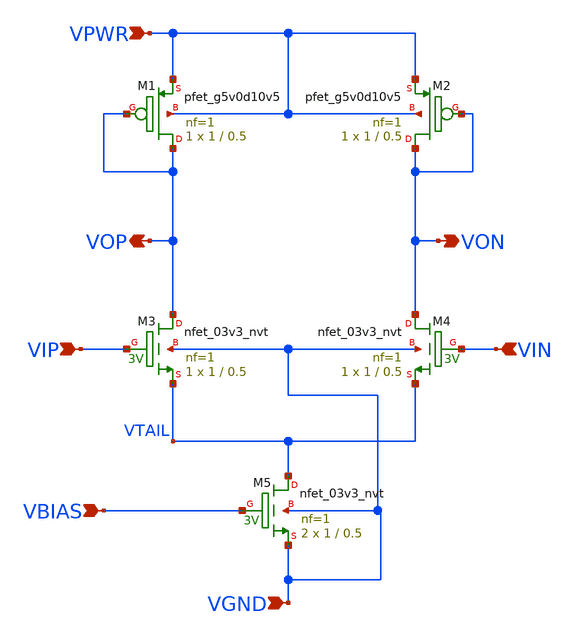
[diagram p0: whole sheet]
** sch_path: xschem/gm-c_filter/ltp.sch
**.subckt ltp VBIAS VIP VPWR VIN VGND VON VOP
*.ipin VBIAS
*.ipin VIP
*.ipin VPWR
*.ipin VIN
*.ipin VGND
*.opin VON
*.opin VOP
XM1 VOP VOP VPWR VPWR sky130_fd_pr__pfet_g5v0d10v5 L=0.5 W=1 nf=1 ad='int((nf+1)/2) * W/nf * 0.29' as='int((nf+2)/2) * W/nf * 0.29'
+ pd='2*int((nf+1)/2) * (W/nf + 0.29)' ps='2*int((nf+2)/2) * (W/nf + 0.29)' nrd='0.29 / W' nrs='0.29 / W'
+ sa=0 sb=0 sd=0 mult=1 m=1
XM2 VON VON VPWR VPWR sky130_fd_pr__pfet_g5v0d10v5 L=0.5 W=1 nf=1 ad='int((nf+1)/2) * W/nf * 0.29' as='int((nf+2)/2) * W/nf * 0.29'
+ pd='2*int((nf+1)/2) * (W/nf + 0.29)' ps='2*int((nf+2)/2) * (W/nf + 0.29)' nrd='0.29 / W' nrs='0.29 / W'
+ sa=0 sb=0 sd=0 mult=1 m=1
XM3 VOP VIP VTAIL VGND sky130_fd_pr__nfet_03v3_nvt L=0.5 W=1 nf=1 ad='int((nf+1)/2) * W/nf * 0.29' as='int((nf+2)/2) * W/nf * 0.29'
+ pd='2*int((nf+1)/2) * (W/nf + 0.29)' ps='2*int((nf+2)/2) * (W/nf + 0.29)' nrd='0.29 / W' nrs='0.29 / W'
+ sa=0 sb=0 sd=0 mult=1 m=1
XM4 VON VIN VTAIL VGND sky130_fd_pr__nfet_03v3_nvt L=0.5 W=1 nf=1 ad='int((nf+1)/2) * W/nf * 0.29' as='int((nf+2)/2) * W/nf * 0.29'
+ pd='2*int((nf+1)/2) * (W/nf + 0.29)' ps='2*int((nf+2)/2) * (W/nf + 0.29)' nrd='0.29 / W' nrs='0.29 / W'
+ sa=0 sb=0 sd=0 mult=1 m=1
XM5 VTAIL VBIAS VGND VGND sky130_fd_pr__nfet_03v3_nvt L=0.5 W=1 nf=1 ad='int((nf+1)/2) * W/nf * 0.29'
+ as='int((nf+2)/2) * W/nf * 0.29' pd='2*int((nf+1)/2) * (W/nf + 0.29)' ps='2*int((nf+2)/2) * (W/nf + 0.29)'
+ nrd='0.29 / W' nrs='0.29 / W' sa=0 sb=0 sd=0 mult=2 m=2
**.ends
.end
